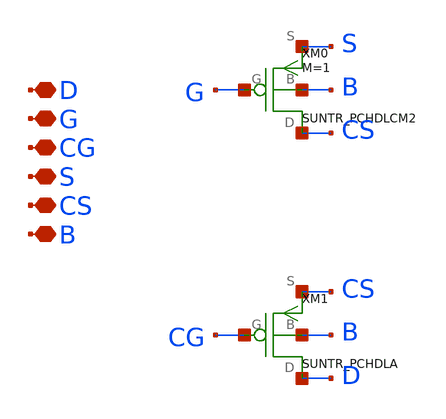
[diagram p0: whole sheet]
** sch_path: ip/sun_tr_sky130nm/design/SUN_TR_SKY130NM/SUNTR_CPCHDLCM2.sch
**.subckt SUNTR_CPCHDLCM2 D G CG S CS B
*.iopin D
*.iopin G
*.iopin CG
*.iopin S
*.iopin CS
*.iopin B
XM0 CS G S B SUNTR_PCHDLCM2 xoffset=0 yoffset=0 angle=0 M=1
XM1 D CG CS B SUNTR_PCHDLA xoffset=0 yoffset=0 angle=0
**.ends
.end
